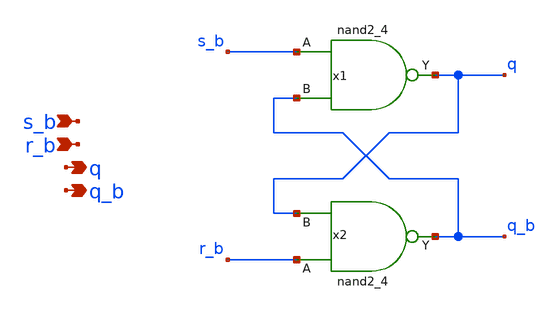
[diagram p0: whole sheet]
** sch_path: design/analog_modulator/schematic/rs_b_latch.sch
**.subckt rs_b_latch s_b r_b q q_b
*.ipin s_b
*.ipin r_b
*.opin q
*.opin q_b
x1 s_b q_b VSS VSS VDD VDD q sky130_fd_sc_hd__nand2_4
x2 r_b q VSS VSS VDD VDD q_b sky130_fd_sc_hd__nand2_4
**.ends
.end
